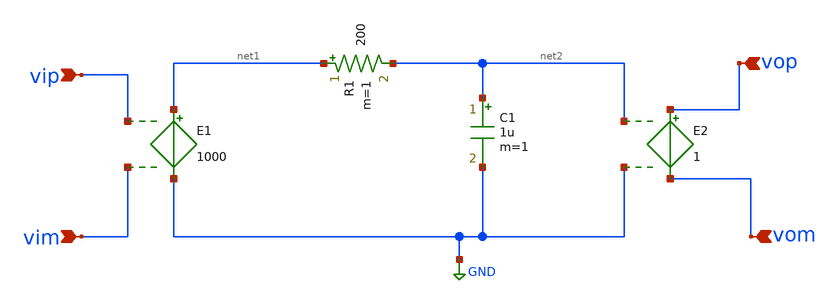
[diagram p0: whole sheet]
** sch_path: work/xschem/buffer.sch
**.subckt buffer vop vom vim vip
*.ipin vop
*.ipin vom
*.ipin vim
*.ipin vip
E1 net1 GND vip vim 1000
R1 net1 net2 200 m=1
C1 net2 GND 1u m=1
E2 vop vom net2 GND 1
**.ends
.GLOBAL GND
.end
